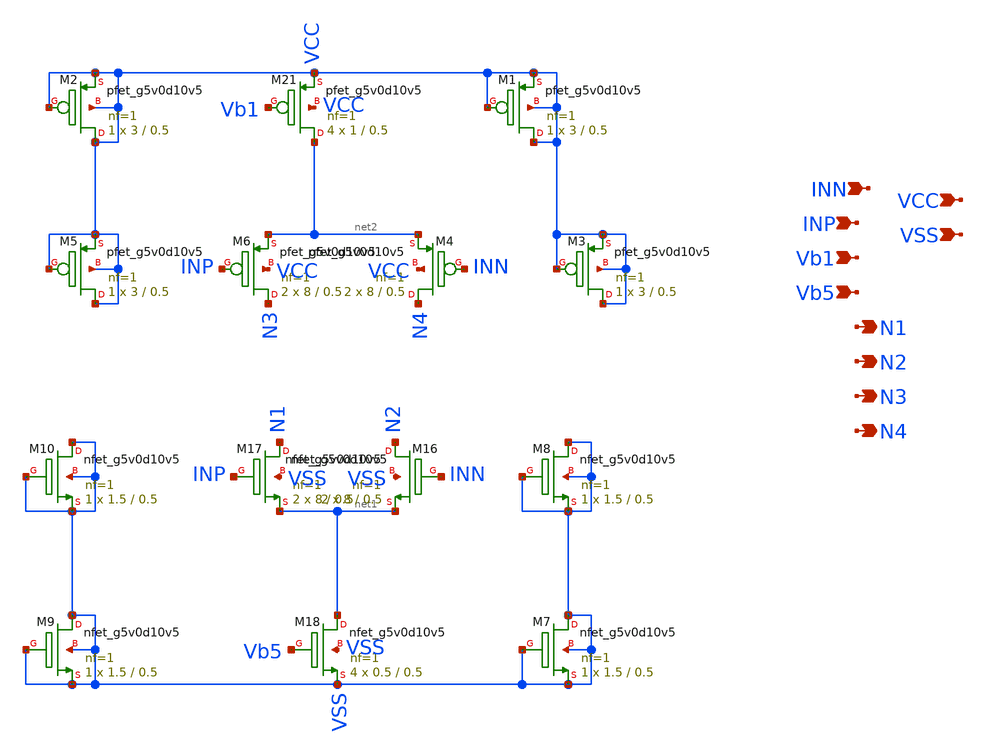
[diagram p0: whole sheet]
** sch_path: latest_working_comparator/input_stage.sch
**.subckt input_stage INN INP Vb1 Vb5 N1 N2 N3 N4 VCC VSS
*.ipin INN
*.ipin INP
*.ipin Vb1
*.ipin Vb5
*.opin N1
*.opin N2
*.opin N3
*.opin N4
*.ipin VCC
*.ipin VSS
XM16 N2 INN net1 VSS sky130_fd_pr__nfet_g5v0d10v5 L=0.5 W=8 nf=1 ad='int((nf+1)/2) * W/nf * 0.29' as='int((nf+2)/2) * W/nf * 0.29'
+ pd='2*int((nf+1)/2) * (W/nf + 0.29)' ps='2*int((nf+2)/2) * (W/nf + 0.29)' nrd='0.29 / W' nrs='0.29 / W'
+ sa=0 sb=0 sd=0 mult=2 m=2
XM17 N1 INP net1 VSS sky130_fd_pr__nfet_g5v0d10v5 L=0.5 W=8 nf=1 ad='int((nf+1)/2) * W/nf * 0.29' as='int((nf+2)/2) * W/nf * 0.29'
+ pd='2*int((nf+1)/2) * (W/nf + 0.29)' ps='2*int((nf+2)/2) * (W/nf + 0.29)' nrd='0.29 / W' nrs='0.29 / W'
+ sa=0 sb=0 sd=0 mult=2 m=2
XM6 N3 INP net2 VCC sky130_fd_pr__pfet_g5v0d10v5 L=0.5 W=8 nf=1 ad='int((nf+1)/2) * W/nf * 0.29' as='int((nf+2)/2) * W/nf * 0.29'
+ pd='2*int((nf+1)/2) * (W/nf + 0.29)' ps='2*int((nf+2)/2) * (W/nf + 0.29)' nrd='0.29 / W' nrs='0.29 / W'
+ sa=0 sb=0 sd=0 mult=2 m=2
XM21 net2 Vb1 VCC VCC sky130_fd_pr__pfet_g5v0d10v5 L=0.5 W=1 nf=1 ad='int((nf+1)/2) * W/nf * 0.29' as='int((nf+2)/2) * W/nf * 0.29'
+ pd='2*int((nf+1)/2) * (W/nf + 0.29)' ps='2*int((nf+2)/2) * (W/nf + 0.29)' nrd='0.29 / W' nrs='0.29 / W'
+ sa=0 sb=0 sd=0 mult=4 m=4
XM18 net1 Vb5 VSS VSS sky130_fd_pr__nfet_g5v0d10v5 L=0.5 W=0.5 nf=1 ad='int((nf+1)/2) * W/nf * 0.29'
+ as='int((nf+2)/2) * W/nf * 0.29' pd='2*int((nf+1)/2) * (W/nf + 0.29)' ps='2*int((nf+2)/2) * (W/nf + 0.29)'
+ nrd='0.29 / W' nrs='0.29 / W' sa=0 sb=0 sd=0 mult=4 m=4
XM4 N4 INN net2 VCC sky130_fd_pr__pfet_g5v0d10v5 L=0.5 W=8 nf=1 ad='int((nf+1)/2) * W/nf * 0.29' as='int((nf+2)/2) * W/nf * 0.29'
+ pd='2*int((nf+1)/2) * (W/nf + 0.29)' ps='2*int((nf+2)/2) * (W/nf + 0.29)' nrd='0.29 / W' nrs='0.29 / W'
+ sa=0 sb=0 sd=0 mult=2 m=2
XM1 VCC VCC VCC VCC sky130_fd_pr__pfet_g5v0d10v5 L=0.5 W=3 nf=1 ad='int((nf+1)/2) * W/nf * 0.29' as='int((nf+2)/2) * W/nf * 0.29'
+ pd='2*int((nf+1)/2) * (W/nf + 0.29)' ps='2*int((nf+2)/2) * (W/nf + 0.29)' nrd='0.29 / W' nrs='0.29 / W'
+ sa=0 sb=0 sd=0 mult=1 m=1
XM2 VCC VCC VCC VCC sky130_fd_pr__pfet_g5v0d10v5 L=0.5 W=3 nf=1 ad='int((nf+1)/2) * W/nf * 0.29' as='int((nf+2)/2) * W/nf * 0.29'
+ pd='2*int((nf+1)/2) * (W/nf + 0.29)' ps='2*int((nf+2)/2) * (W/nf + 0.29)' nrd='0.29 / W' nrs='0.29 / W'
+ sa=0 sb=0 sd=0 mult=1 m=1
XM3 VCC VCC VCC VCC sky130_fd_pr__pfet_g5v0d10v5 L=0.5 W=3 nf=1 ad='int((nf+1)/2) * W/nf * 0.29' as='int((nf+2)/2) * W/nf * 0.29'
+ pd='2*int((nf+1)/2) * (W/nf + 0.29)' ps='2*int((nf+2)/2) * (W/nf + 0.29)' nrd='0.29 / W' nrs='0.29 / W'
+ sa=0 sb=0 sd=0 mult=1 m=1
XM5 VCC VCC VCC VCC sky130_fd_pr__pfet_g5v0d10v5 L=0.5 W=3 nf=1 ad='int((nf+1)/2) * W/nf * 0.29' as='int((nf+2)/2) * W/nf * 0.29'
+ pd='2*int((nf+1)/2) * (W/nf + 0.29)' ps='2*int((nf+2)/2) * (W/nf + 0.29)' nrd='0.29 / W' nrs='0.29 / W'
+ sa=0 sb=0 sd=0 mult=1 m=1
XM7 VSS VSS VSS VSS sky130_fd_pr__nfet_g5v0d10v5 L=0.5 W=1.5 nf=1 ad='int((nf+1)/2) * W/nf * 0.29' as='int((nf+2)/2) * W/nf * 0.29'
+ pd='2*int((nf+1)/2) * (W/nf + 0.29)' ps='2*int((nf+2)/2) * (W/nf + 0.29)' nrd='0.29 / W' nrs='0.29 / W'
+ sa=0 sb=0 sd=0 mult=1 m=1
XM8 VSS VSS VSS VSS sky130_fd_pr__nfet_g5v0d10v5 L=0.5 W=1.5 nf=1 ad='int((nf+1)/2) * W/nf * 0.29' as='int((nf+2)/2) * W/nf * 0.29'
+ pd='2*int((nf+1)/2) * (W/nf + 0.29)' ps='2*int((nf+2)/2) * (W/nf + 0.29)' nrd='0.29 / W' nrs='0.29 / W'
+ sa=0 sb=0 sd=0 mult=1 m=1
XM9 VSS VSS VSS VSS sky130_fd_pr__nfet_g5v0d10v5 L=0.5 W=1.5 nf=1 ad='int((nf+1)/2) * W/nf * 0.29' as='int((nf+2)/2) * W/nf * 0.29'
+ pd='2*int((nf+1)/2) * (W/nf + 0.29)' ps='2*int((nf+2)/2) * (W/nf + 0.29)' nrd='0.29 / W' nrs='0.29 / W'
+ sa=0 sb=0 sd=0 mult=1 m=1
XM10 VSS VSS VSS VSS sky130_fd_pr__nfet_g5v0d10v5 L=0.5 W=1.5 nf=1 ad='int((nf+1)/2) * W/nf * 0.29' as='int((nf+2)/2) * W/nf * 0.29'
+ pd='2*int((nf+1)/2) * (W/nf + 0.29)' ps='2*int((nf+2)/2) * (W/nf + 0.29)' nrd='0.29 / W' nrs='0.29 / W'
+ sa=0 sb=0 sd=0 mult=1 m=1
**.ends
.end
